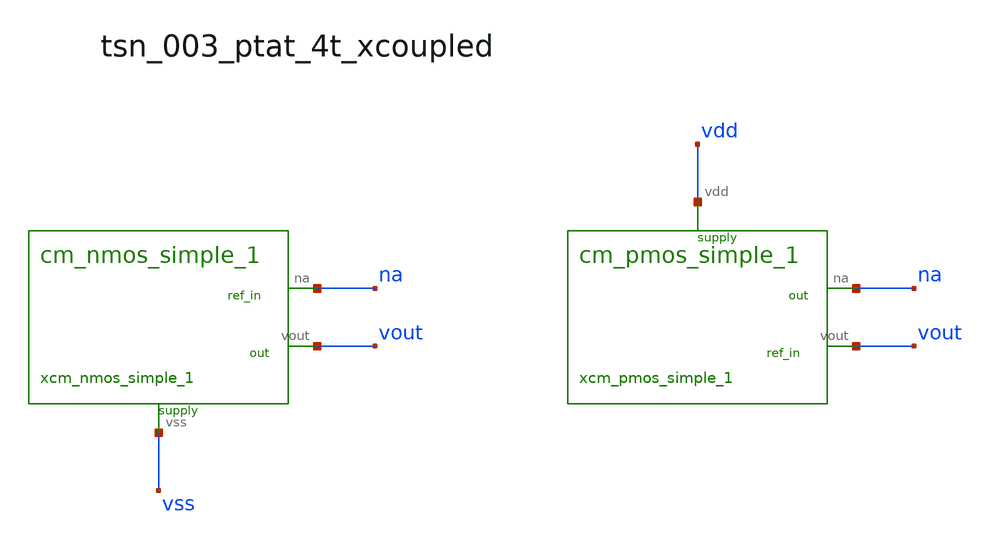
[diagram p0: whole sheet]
** sch_path: analog-db/raw/tsn_003_ptat_4t_xcoupled/hier/tsn_003_ptat_4t_xcoupled.sch
**.subckt tsn_003_ptat_4t_xcoupled
xcm_nmos_simple_1 na vout vss cm_nmos_simple_1
xcm_pmos_simple_1 na vout vdd cm_pmos_simple_1
**.ends

* expanding   symbol:  blocks/cm_nmos_simple_1.sym # of pins=3
** sym_path: analog-db/raw/tsn_003_ptat_4t_xcoupled/hier/blocks/cm_nmos_simple_1.sym
** sch_path: analog-db/raw/tsn_003_ptat_4t_xcoupled/hier/blocks/cm_nmos_simple_1.sch
.subckt cm_nmos_simple_1 na vout vss
*.iopin vss
*.opin vout
*.opin na
XM0 vout na vss vss sg13_lv_nmos w=x_dut_xm0_w l=x_dut_xm0_l ng=1 m=x_dut_xm0_m
XM1 na na vss vss sg13_lv_nmos w=x_dut_xm1_w l=x_dut_xm1_l ng=1 m=x_dut_xm1_m
.ends


* expanding   symbol:  blocks/cm_pmos_simple_1.sym # of pins=3
** sym_path: analog-db/raw/tsn_003_ptat_4t_xcoupled/hier/blocks/cm_pmos_simple_1.sym
** sch_path: analog-db/raw/tsn_003_ptat_4t_xcoupled/hier/blocks/cm_pmos_simple_1.sch
.subckt cm_pmos_simple_1 na vout vdd
*.iopin vdd
*.opin vout
*.opin na
XM3 vout vout vdd vdd sg13_lv_pmos w=x_dut_xm3_w l=x_dut_xm3_l ng=1 m=x_dut_xm3_m
XM4 na vout vdd vdd sg13_lv_pmos w=x_dut_xm4_w l=x_dut_xm4_l ng=1 m=x_dut_xm4_m
.ends

.end
